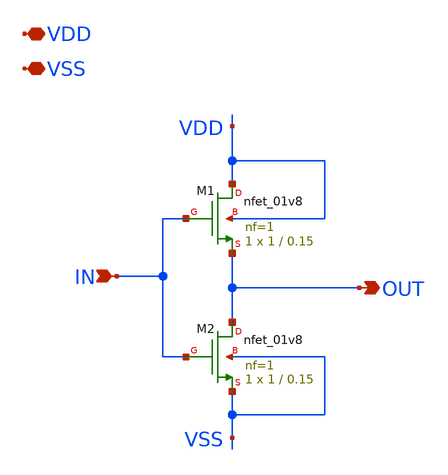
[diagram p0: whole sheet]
** sch_path: xschem/inverter.sch
**.subckt inverter VDD VSS IN OUT
*.iopin VDD
*.iopin VSS
*.ipin IN
*.opin OUT
XM2 OUT IN VSS VSS sky130_fd_pr__nfet_01v8 L=0.15 W=1 nf=1 ad='int((nf+1)/2) * W/nf * 0.29' as='int((nf+2)/2) * W/nf * 0.29'
+ pd='2*int((nf+1)/2) * (W/nf + 0.29)' ps='2*int((nf+2)/2) * (W/nf + 0.29)' nrd='0.29 / W' nrs='0.29 / W'
+ sa=0 sb=0 sd=0 mult=1 m=1
XM1 VDD IN OUT VDD sky130_fd_pr__nfet_01v8 L=0.15 W=1 nf=1 ad='int((nf+1)/2) * W/nf * 0.29' as='int((nf+2)/2) * W/nf * 0.29'
+ pd='2*int((nf+1)/2) * (W/nf + 0.29)' ps='2*int((nf+2)/2) * (W/nf + 0.29)' nrd='0.29 / W' nrs='0.29 / W'
+ sa=0 sb=0 sd=0 mult=1 m=1
**.ends
.end
